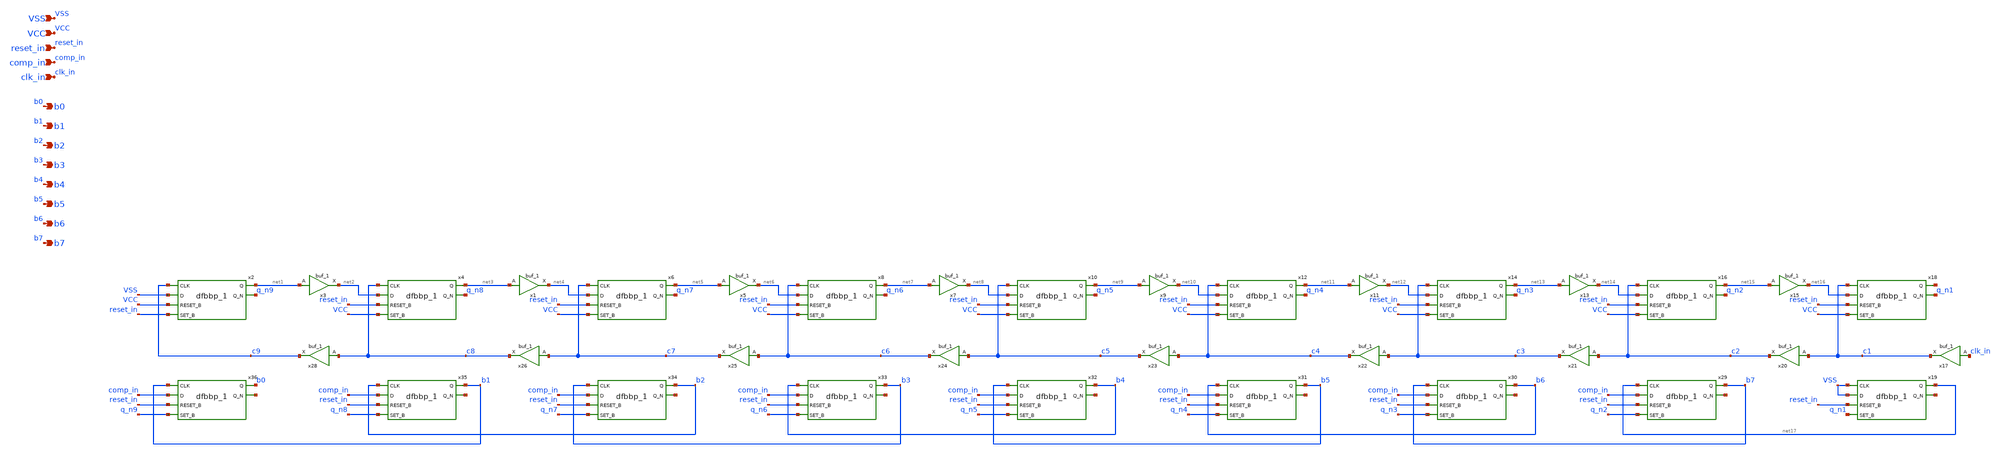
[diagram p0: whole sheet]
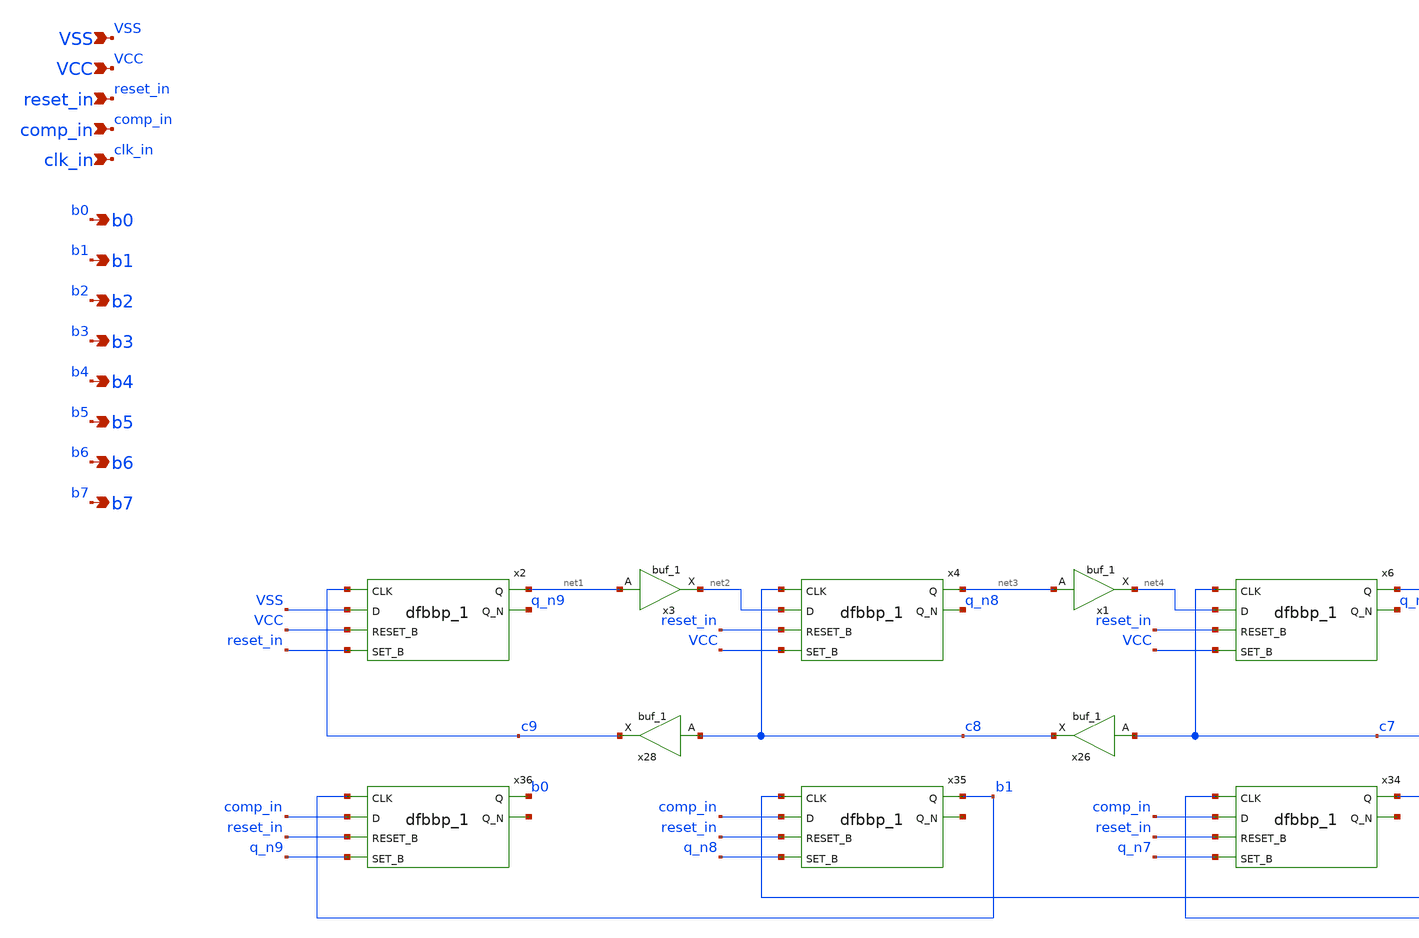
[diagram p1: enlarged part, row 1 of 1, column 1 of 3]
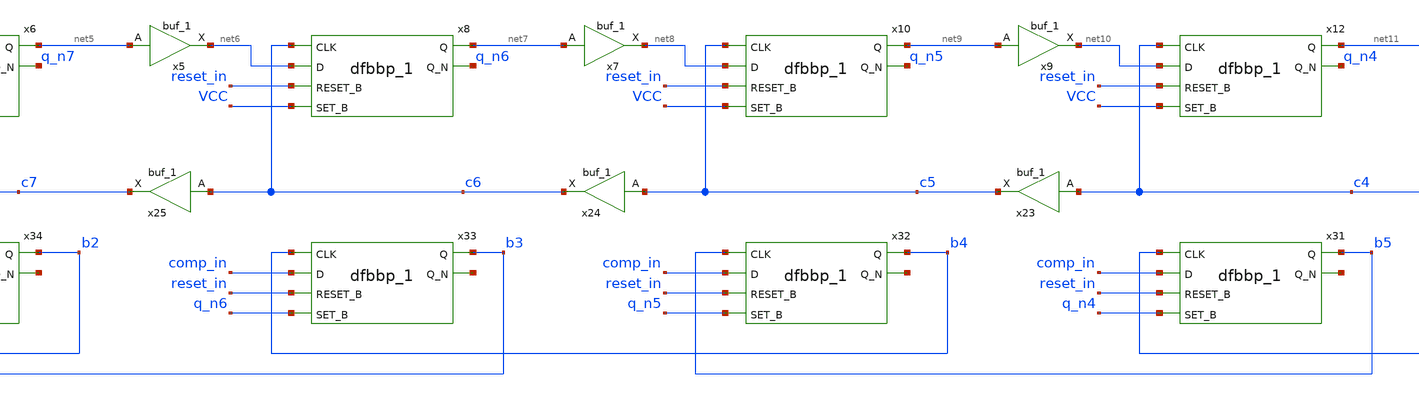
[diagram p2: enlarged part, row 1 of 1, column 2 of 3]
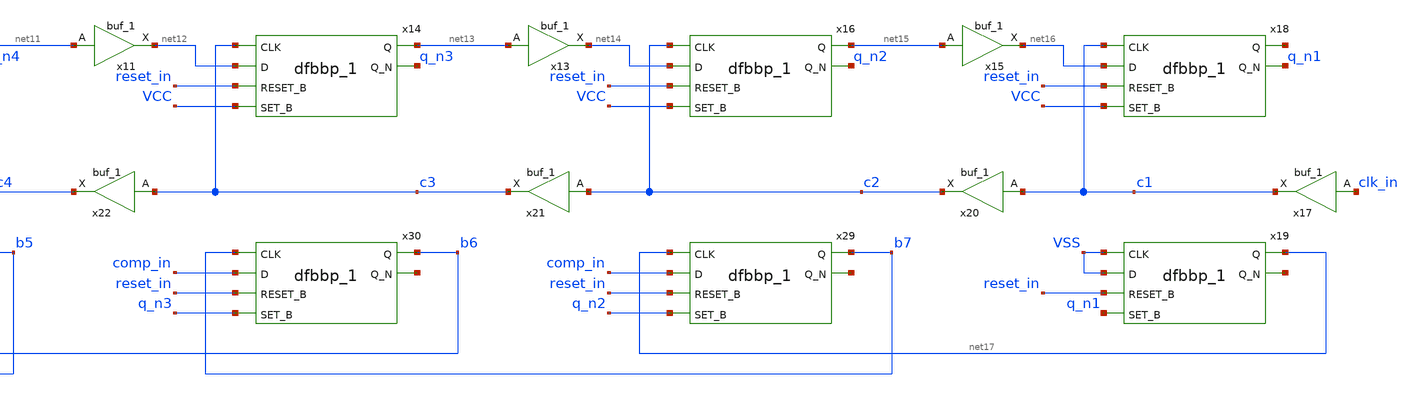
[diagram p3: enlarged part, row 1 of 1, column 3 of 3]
** sch_path: xschem/sar.sch
.lib $::SKYWATER_MODELS/sky130.lib.spice tt
.include $::SKYWATER_STDCELLS/sky130_fd_sc_hd.spice

**.subckt sar b7 b6 b5 b4 b3 b2 b1 b0 comp_in clk_in reset_in VCC VSS
*.opin b7
*.opin b6
*.opin b5
*.opin b4
*.opin b3
*.opin b2
*.opin b1
*.opin b0
*.ipin comp_in
*.ipin clk_in
*.ipin reset_in
*.ipin VCC
*.ipin VSS
x2 c9 VSS VCC reset_in VSS VSS VCC VCC net1 q_n9 sky130_fd_sc_hd__dfbbp_1
x3 net1 VSS VSS VCC VCC net2 sky130_fd_sc_hd__buf_1
x4 c8 net2 reset_in VCC VSS VSS VCC VCC net3 q_n8 sky130_fd_sc_hd__dfbbp_1
x6 c7 net4 reset_in VCC VSS VSS VCC VCC net5 q_n7 sky130_fd_sc_hd__dfbbp_1
x8 c6 net6 reset_in VCC VSS VSS VCC VCC net7 q_n6 sky130_fd_sc_hd__dfbbp_1
x10 c5 net8 reset_in VCC VSS VSS VCC VCC net9 q_n5 sky130_fd_sc_hd__dfbbp_1
x12 c4 net10 reset_in VCC VSS VSS VCC VCC net11 q_n4 sky130_fd_sc_hd__dfbbp_1
x14 c3 net12 reset_in VCC VSS VSS VCC VCC net13 q_n3 sky130_fd_sc_hd__dfbbp_1
x16 c2 net14 reset_in VCC VSS VSS VCC VCC net15 q_n2 sky130_fd_sc_hd__dfbbp_1
x18 c1 net16 reset_in VCC VSS VSS VCC VCC net18 q_n1 sky130_fd_sc_hd__dfbbp_1
x19 VSS VSS reset_in q_n1 VSS VSS VCC VCC net17 net19 sky130_fd_sc_hd__dfbbp_1
x28 c8 VSS VSS VCC VCC c9 sky130_fd_sc_hd__buf_1
x29 net17 comp_in reset_in q_n2 VSS VSS VCC VCC b7 net20 sky130_fd_sc_hd__dfbbp_1
x30 b7 comp_in reset_in q_n3 VSS VSS VCC VCC b6 net21 sky130_fd_sc_hd__dfbbp_1
x31 b6 comp_in reset_in q_n4 VSS VSS VCC VCC b5 net22 sky130_fd_sc_hd__dfbbp_1
x32 b5 comp_in reset_in q_n5 VSS VSS VCC VCC b4 net23 sky130_fd_sc_hd__dfbbp_1
x33 b4 comp_in reset_in q_n6 VSS VSS VCC VCC b3 net24 sky130_fd_sc_hd__dfbbp_1
x34 b3 comp_in reset_in q_n7 VSS VSS VCC VCC b2 net25 sky130_fd_sc_hd__dfbbp_1
x35 b2 comp_in reset_in q_n8 VSS VSS VCC VCC b1 net26 sky130_fd_sc_hd__dfbbp_1
x36 b1 comp_in reset_in q_n9 VSS VSS VCC VCC b0 net27 sky130_fd_sc_hd__dfbbp_1
x1 net3 VSS VSS VCC VCC net4 sky130_fd_sc_hd__buf_1
x5 net5 VSS VSS VCC VCC net6 sky130_fd_sc_hd__buf_1
x7 net7 VSS VSS VCC VCC net8 sky130_fd_sc_hd__buf_1
x9 net9 VSS VSS VCC VCC net10 sky130_fd_sc_hd__buf_1
x11 net11 VSS VSS VCC VCC net12 sky130_fd_sc_hd__buf_1
x13 net13 VSS VSS VCC VCC net14 sky130_fd_sc_hd__buf_1
x15 net15 VSS VSS VCC VCC net16 sky130_fd_sc_hd__buf_1
x17 clk_in VSS VSS VCC VCC c1 sky130_fd_sc_hd__buf_1
x20 c1 VSS VSS VCC VCC c2 sky130_fd_sc_hd__buf_1
x21 c2 VSS VSS VCC VCC c3 sky130_fd_sc_hd__buf_1
x22 c3 VSS VSS VCC VCC c4 sky130_fd_sc_hd__buf_1
x23 c4 VSS VSS VCC VCC c5 sky130_fd_sc_hd__buf_1
x24 c5 VSS VSS VCC VCC c6 sky130_fd_sc_hd__buf_1
x25 c6 VSS VSS VCC VCC c7 sky130_fd_sc_hd__buf_1
x26 c7 VSS VSS VCC VCC c8 sky130_fd_sc_hd__buf_1
**** begin user architecture code


.options acct list
.temp 25
.control
  save all
  savecurrents
  op
  write sar.raw
  reset
  set appendwrite
  save all
  tran 0.1n 12u uic
  write sar.raw
  reset
  quit 0
.endc

**** end user architecture code
**.ends
.end
